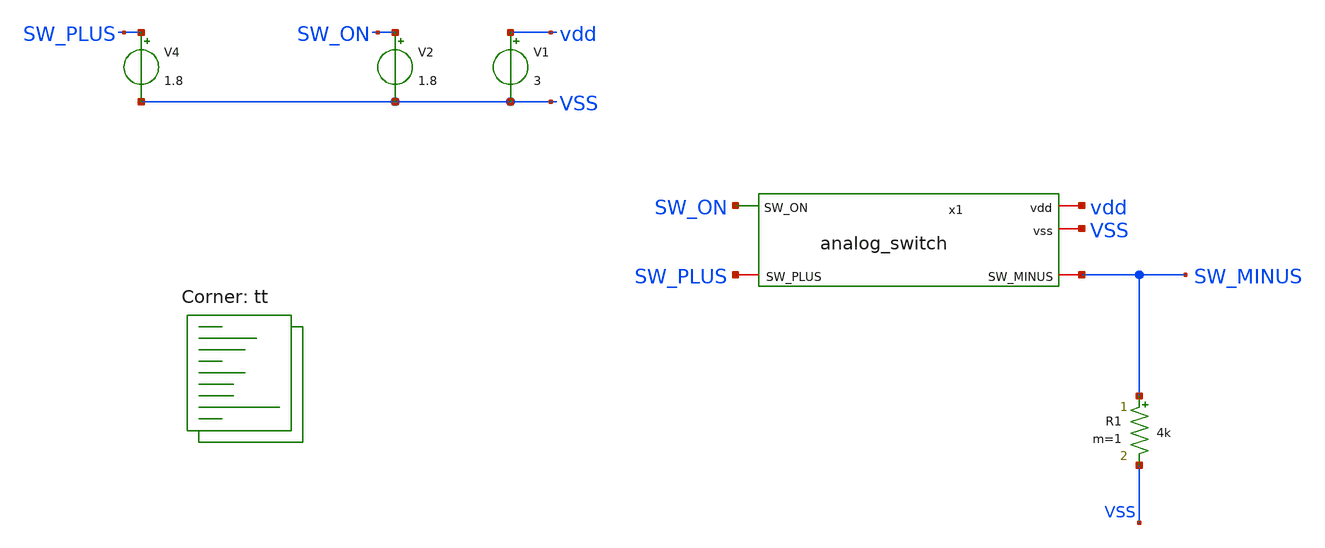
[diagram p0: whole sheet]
** sch_path: xschem/sw_tb_simple.sch
**.subckt sw_tb_simple
R1 SW_MINUS VSS 4k m=1
x1 vdd VSS SW_ON SW_PLUS SW_MINUS analog_switch
V1 vdd VSS 3
V2 SW_ON VSS 1.8
V4 SW_PLUS VSS 1.8
**** begin user architecture code
.lib $::SKYWATER_MODELS/sky130.lib.spice tt

.options gmin=1e-12 abstol=1e-12 reltol=1e-3
.options method=gear
.options maxord=2
R_SW_ON sw_on x1.nsw_on 1
R_LOAD sw_minus 0 1MEG
.control
.IC V(sw_on)=1.8 V(sw_plus)=1.8 V(sw_minus)=0
tran 100p 200n uic
write testbench.raw
.endc


**** end user architecture code
**.ends

* expanding   symbol:  analog_switch.sym # of pins=5
** sym_path: xschem/analog_switch.sym
** sch_path: xschem/analog_switch.sch
.subckt analog_switch vdd vss SW_ON SW_PLUS SW_MINUS
*.iopin vdd
*.iopin vss
*.ipin SW_ON
*.iopin SW_MINUS
*.iopin SW_PLUS
XM1 SW_PLUS SW_ON_BUF SW_MINUS SW_MINUS sky130_fd_pr__nfet_g5v0d10v5 L=15 W=16 nf=1 ad='int((1 + 1)/2) * 16 / 1 * 0.29'
+ as='int((1 + 2)/2) * 16 / 1 * 0.29' pd='2*int((1 + 1)/2) * (16 / 1 + 0.29)' ps='2*int((1 + 2)/2) * (16 / 1 + 0.29)'
+ nrd='0.29 / 16 ' nrs='0.29 / 16 ' sa=0 sb=0 sd=0 mult=1 m=1
XM3 SW_MINUS nSW_ON SW_PLUS SW_PLUS sky130_fd_pr__pfet_g5v0d10v5 L=15 W=16 nf=1 ad='int((1 + 1)/2) * 16 / 1 * 0.29'
+ as='int((1 + 2)/2) * 16 / 1 * 0.29' pd='2*int((1 + 1)/2) * (16 / 1 + 0.29)' ps='2*int((1 + 2)/2) * (16 / 1 + 0.29)'
+ nrd='0.29 / 16 ' nrs='0.29 / 16 ' sa=0 sb=0 sd=0 mult=1 m=1
XM2 SW_MINUS nSW_ON SW_MINUS SW_MINUS sky130_fd_pr__nfet_g5v0d10v5 L=15 W=16 nf=1 ad='int((1 + 1)/2) * 16 / 1 * 0.29'
+ as='int((1 + 2)/2) * 16 / 1 * 0.29' pd='2*int((1 + 1)/2) * (16 / 1 + 0.29)' ps='2*int((1 + 2)/2) * (16 / 1 + 0.29)'
+ nrd='0.29 / 16 ' nrs='0.29 / 16 ' sa=0 sb=0 sd=0 mult=1 m=1
XM4 SW_MINUS SW_ON_BUF SW_MINUS SW_MINUS sky130_fd_pr__pfet_g5v0d10v5 L=15 W=16 nf=1 ad='int((1 + 1)/2) * 16 / 1 * 0.29'
+ as='int((1 + 2)/2) * 16 / 1 * 0.29' pd='2*int((1 + 1)/2) * (16 / 1 + 0.29)' ps='2*int((1 + 2)/2) * (16 / 1 + 0.29)'
+ nrd='0.29 / 16 ' nrs='0.29 / 16 ' sa=0 sb=0 sd=0 mult=1 m=1
XM6 SW_ON_BUF net1 vss vss sky130_fd_pr__nfet_g5v0d10v5 L=0.5 W=2 nf=1 ad='int((1 + 1)/2) * 2 / 1 * 0.29'
+ as='int((1 + 2)/2) * 2 / 1 * 0.29' pd='2*int((1 + 1)/2) * (2 / 1 + 0.29)' ps='2*int((1 + 2)/2) * (2 / 1 + 0.29)'
+ nrd='0.29 / 2 ' nrs='0.29 / 2 ' sa=0 sb=0 sd=0 mult=1 m=1
XM7 SW_ON_BUF net1 vdd vdd sky130_fd_pr__pfet_g5v0d10v5 L=0.5 W=2 nf=1 ad='int((1 + 1)/2) * 2 / 1 * 0.29'
+ as='int((1 + 2)/2) * 2 / 1 * 0.29' pd='2*int((1 + 1)/2) * (2 / 1 + 0.29)' ps='2*int((1 + 2)/2) * (2 / 1 + 0.29)'
+ nrd='0.29 / 2 ' nrs='0.29 / 2 ' sa=0 sb=0 sd=0 mult=1 m=1
XM8 net1 SW_ON vss vss sky130_fd_pr__nfet_g5v0d10v5 L=0.5 W=2 nf=1 ad='int((1 + 1)/2) * 2 / 1 * 0.29'
+ as='int((1 + 2)/2) * 2 / 1 * 0.29' pd='2*int((1 + 1)/2) * (2 / 1 + 0.29)' ps='2*int((1 + 2)/2) * (2 / 1 + 0.29)'
+ nrd='0.29 / 2 ' nrs='0.29 / 2 ' sa=0 sb=0 sd=0 mult=1 m=1
XM10 net1 SW_ON vdd vdd sky130_fd_pr__pfet_g5v0d10v5 L=0.5 W=2 nf=1 ad='int((1 + 1)/2) * 2 / 1 * 0.29'
+ as='int((1 + 2)/2) * 2 / 1 * 0.29' pd='2*int((1 + 1)/2) * (2 / 1 + 0.29)' ps='2*int((1 + 2)/2) * (2 / 1 + 0.29)'
+ nrd='0.29 / 2 ' nrs='0.29 / 2 ' sa=0 sb=0 sd=0 mult=1 m=1
XM5 nSW_ON SW_ON_BUF vss vss sky130_fd_pr__nfet_g5v0d10v5 L=0.5 W=2 nf=1 ad='int((1 + 1)/2) * 2 / 1 * 0.29'
+ as='int((1 + 2)/2) * 2 / 1 * 0.29' pd='2*int((1 + 1)/2) * (2 / 1 + 0.29)' ps='2*int((1 + 2)/2) * (2 / 1 + 0.29)'
+ nrd='0.29 / 2 ' nrs='0.29 / 2 ' sa=0 sb=0 sd=0 mult=1 m=1
XM9 nSW_ON SW_ON_BUF vdd vdd sky130_fd_pr__pfet_g5v0d10v5 L=0.5 W=2 nf=1 ad='int((1 + 1)/2) * 2 / 1 * 0.29'
+ as='int((1 + 2)/2) * 2 / 1 * 0.29' pd='2*int((1 + 1)/2) * (2 / 1 + 0.29)' ps='2*int((1 + 2)/2) * (2 / 1 + 0.29)'
+ nrd='0.29 / 2 ' nrs='0.29 / 2 ' sa=0 sb=0 sd=0 mult=1 m=1
.ends

.end
